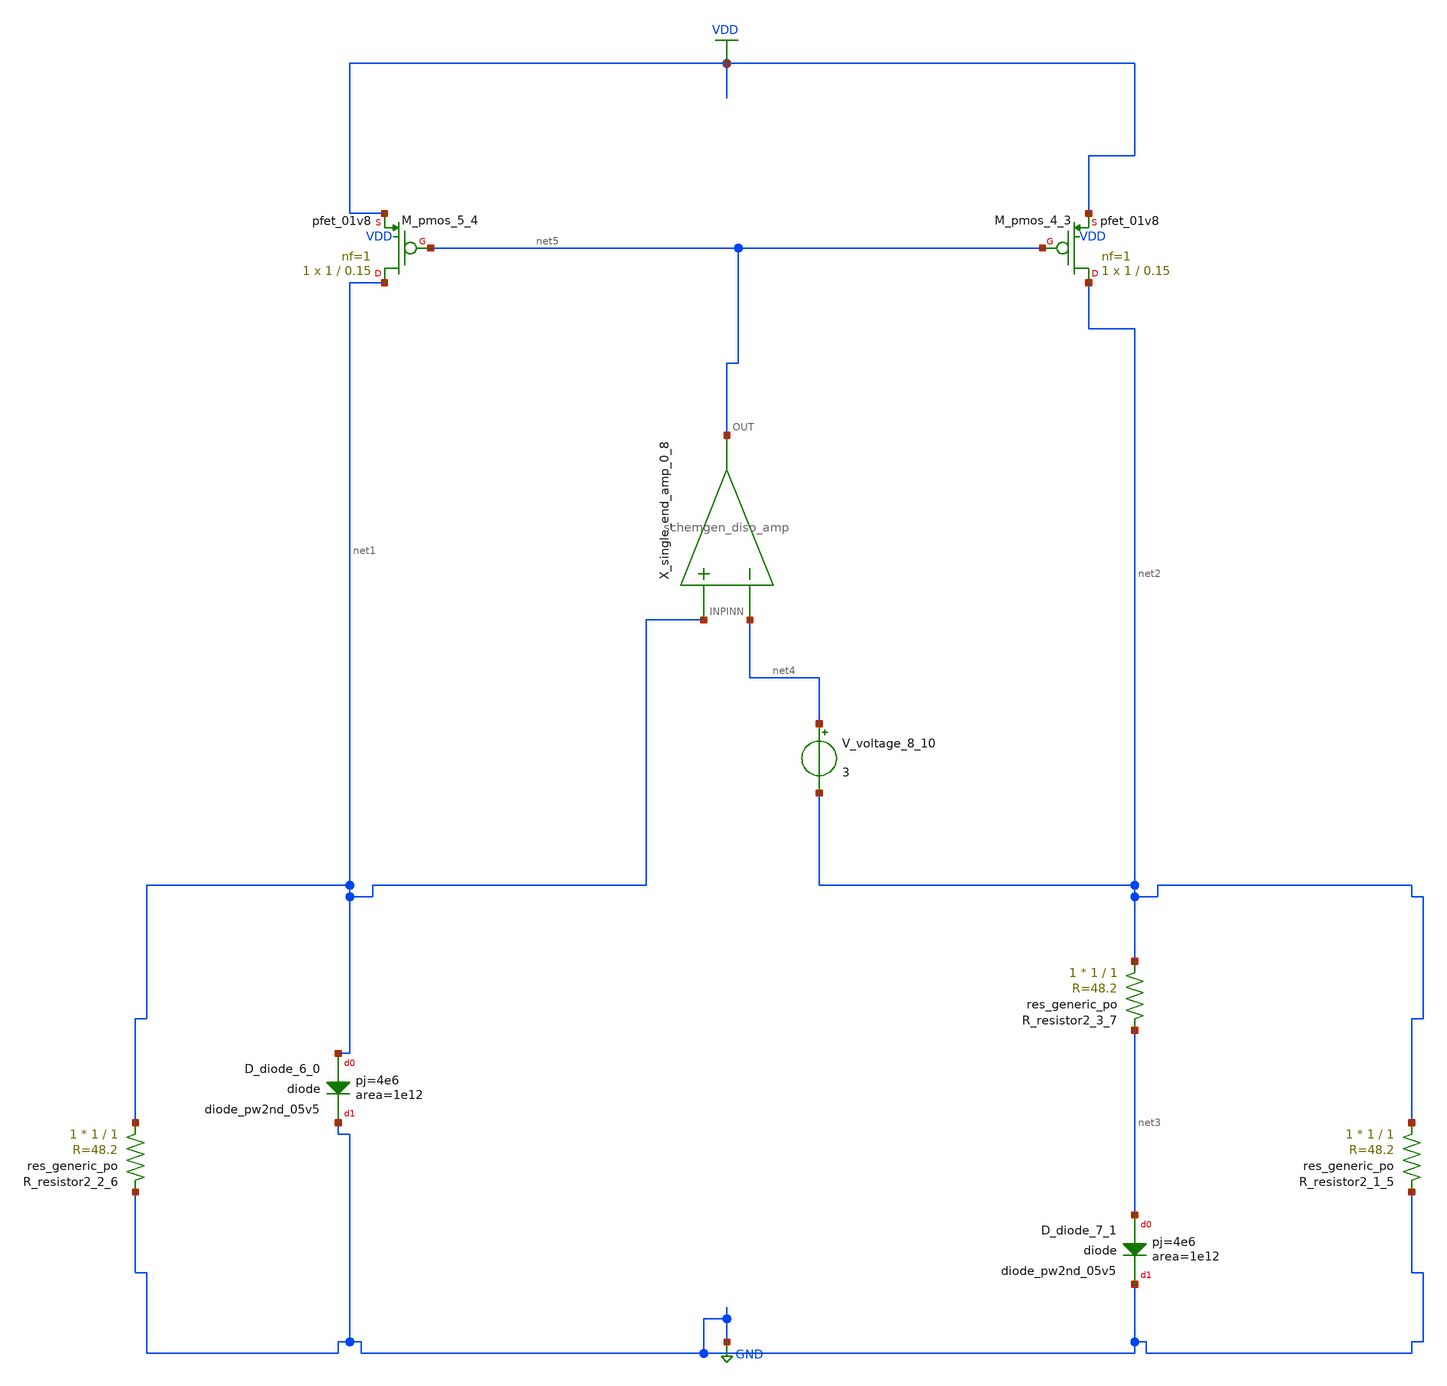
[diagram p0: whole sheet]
** sch_path: schematics/Image2Net/061.sch
**.subckt 061
XD_diode_6_0 net1 GND sky130_fd_pr__diode_pw2nd_05v5 area=1e12 pj=4e6
XD_diode_7_1 net3 GND sky130_fd_pr__diode_pw2nd_05v5 area=1e12 pj=4e6
XM_pmos_4_3 net2 net5 VDD VDD sky130_fd_pr__pfet_01v8 L=0.15 W=1 nf=1 ad='int((1 + 1)/2) * 1 / 1 * 0.29'
+ as='int((1 + 2)/2) * 1 / 1 * 0.29' pd='2*int((1 + 1)/2) * (1 / 1 + 0.29)' ps='2*int((1 + 2)/2) * (1 / 1 + 0.29)'
+ nrd='0.29 / 1 ' nrs='0.29 / 1 ' sa=0 sb=0 sd=0 mult=1 m=1
XM_pmos_5_4 net1 net5 VDD VDD sky130_fd_pr__pfet_01v8 L=0.15 W=1 nf=1 ad='int((1 + 1)/2) * 1 / 1 * 0.29'
+ as='int((1 + 2)/2) * 1 / 1 * 0.29' pd='2*int((1 + 1)/2) * (1 / 1 + 0.29)' ps='2*int((1 + 2)/2) * (1 / 1 + 0.29)'
+ nrd='0.29 / 1 ' nrs='0.29 / 1 ' sa=0 sb=0 sd=0 mult=1 m=1
XR_resistor2_1_5 net2 GND sky130_fd_pr__res_generic_po W=1 L=1 m=1
XR_resistor2_2_6 net1 GND sky130_fd_pr__res_generic_po W=1 L=1 m=1
XR_resistor2_3_7 net2 net3 sky130_fd_pr__res_generic_po W=1 L=1 m=1
X_single_end_amp_0_8 net1 net4 net5 schemgen_diso_amp
V_voltage_8_10 net4 net2 3
**.ends

* expanding   symbol:  schemgen_diso_amp.sym # of pins=3
** sym_path: symbols/schemgen_diso_amp.sym
.subckt schemgen_diso_amp INP INN OUT
* SchemGen ideal op-amp: Vout = 1e5 * (V(INP) - V(INN))
E1 OUT 0 INP INN 1e5
.ends schemgen_diso_amp
.GLOBAL GND
.GLOBAL VDD
.end
